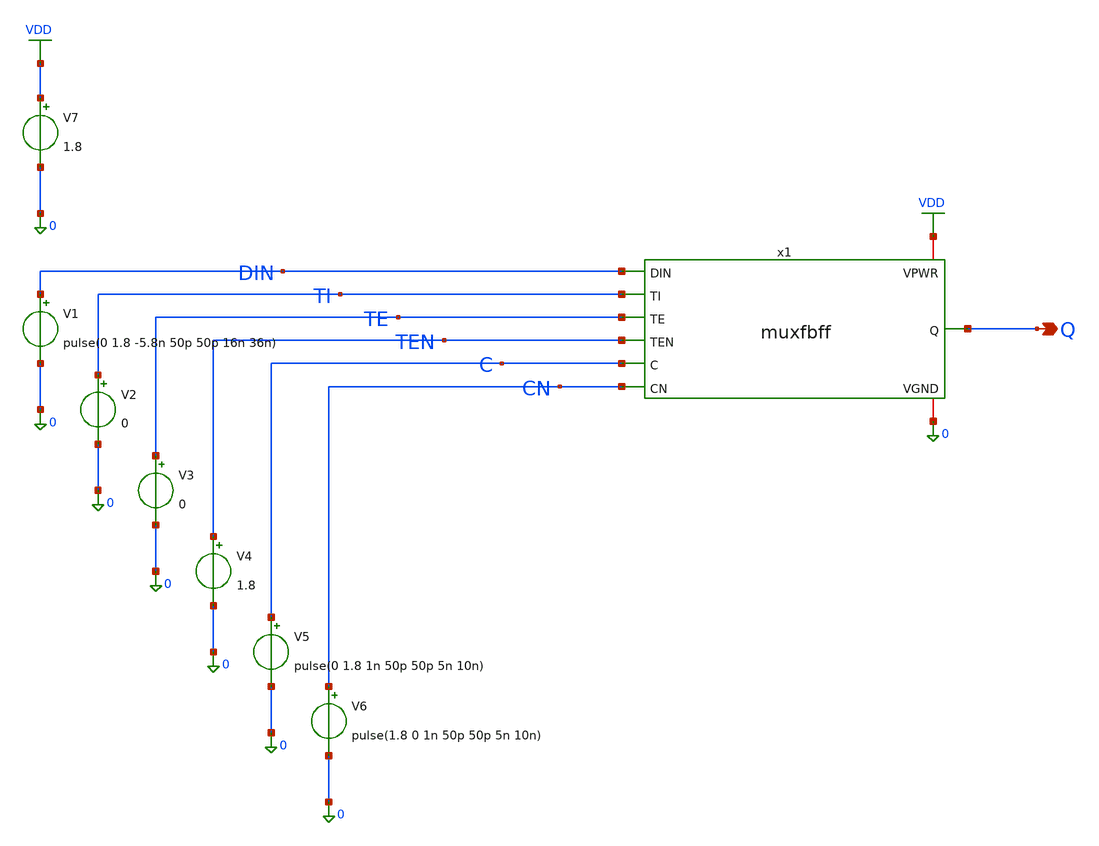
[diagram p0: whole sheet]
** sch_path: muxfbff/muxfbff_tb.sch
**.subckt muxfbff_tb Q
*.opin Q
x1 VDD 0 Q DIN TI TE TEN C CN muxfbff
V1 DIN 0 pulse(0 1.8 -5.8n 50p 50p 16n 36n)
V2 TI 0 0
V3 TE 0 0
V4 TEN 0 1.8
V5 C 0 pulse(0 1.8 1n 50p 50p 5n 10n)
V6 CN 0 pulse(1.8 0 1n 50p 50p 5n 10n)
V7 VDD 0 1.8
**** begin user architecture code

** opencircuitdesign pdks install
.lib $::SKYWATER_MODELS/sky130.lib.spice tt




.tran 0.01n 30n
.control
  save all
    run
	meas tran delay TRIG v(C) VAL=0.9 RISE=2 TARG v(Q) VAL=0.9 RISE=1
	print v(c),v(din),v(q) > outputsim.csv
  end
.endc





**** end user architecture code
**.ends
.GLOBAL VDD
.end
